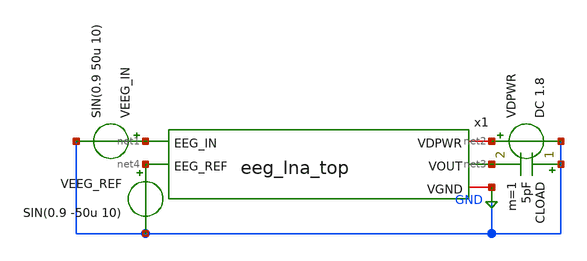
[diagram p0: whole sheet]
** sch_path: xschem/tb_eeg_lna_top.sch
**.subckt tb_eeg_lna_top
x1 net1 net2 net3 GND net4 eeg_lna_top
VDPWR net2 GND DC 1.8
VEEG_REF net4 GND SIN(0.9 -50u 10)
VEEG_IN net1 GND SIN(0.9 50u 10)
CLOAD GND net3 5pF m=1
**** begin user architecture code


.lib /foss/pdks/sky130A/libs.tech/ngspice/sky130.lib.spice tt

* =====================================================
* PARAMETERS
* =====================================================

.param VCM=0.9
.param VAMP=50u
.param FREQ=10

.option savecurrents

.control

* =====================================================
* DC OPERATING POINT
* =====================================================

op

print v(vcm)
print v(ota_inp)
print v(ota_inn)
print v(vout)

* =====================================================
* TRANSIENT ANALYSIS
* =====================================================

tran 100u 1

plot v(eeg_in) v(eeg_ref)
plot v(ota_inp) v(ota_inn)
plot v(vout)
plot v(vout)-0.9

* =====================================================
* AC ANALYSIS
* =====================================================

ac dec 100 0.01 1G

plot db(v(vout)/(v(eeg_in)-v(eeg_ref)))

.endc


**** end user architecture code
**.ends

* expanding   symbol:  eeg_lna_top.sym # of pins=5
** sym_path: xschem/eeg_lna_top.sym
** sch_path: xschem/eeg_lna_top.sch
.subckt eeg_lna_top EEG_IN VDPWR VOUT VGND EEG_REF
*.ipin EEG_IN
*.ipin EEG_REF
*.iopin VDPWR
*.iopin VGND
*.opin VOUT
XCIN_P EEG_IN OTA_INP sky130_fd_pr__cap_mim_m3_1 W=40 L=40 MF=1 m=1
XCIN_N EEG_REF OTA_INN sky130_fd_pr__cap_mim_m3_1 W=40 L=40 MF=1 m=1
x_ota net2 VDPWR OTA_INP OTA_INN VOUT VGND ota_5t
x_rpseudo_p net1 VCM OTA_INP pseudo_res_c
x_rpseudo_n net1 VCM OTA_INN pseudo_res_c
x_bias net2 VGND VDPWR bias_gen
x_vcm VDPWR VGND VCM vcm_gen
XCFB VOUT OTA_INN sky130_fd_pr__cap_mim_m3_1 W=20 L=20 MF=1 m=1
.ends


* expanding   symbol:  ota_5t.sym # of pins=6
** sym_path: xschem-new/ota_5t.sym
** sch_path: xschem-new/ota_5t.sch
.subckt ota_5t BIAS_P VDPWR VIN_P VIN_N VOUT VGND
*.ipin VIN_P
*.ipin VIN_N
*.ipin BIAS_P
*.iopin VDPWR
*.iopin VGND
*.opin VOUT
XMDIFF_P net1 VIN_P TAIL_P VDPWR sky130_fd_pr__pfet_01v8 L=4 W=48 nf=1 ad='int((1 + 1)/2) * 48 / 1 * 0.29'
+ as='int((1 + 2)/2) * 48 / 1 * 0.29' pd='2*int((1 + 1)/2) * (48 / 1 + 0.29)' ps='2*int((1 + 2)/2) * (48 / 1 + 0.29)'
+ nrd='0.29 / 48 ' nrs='0.29 / 48 ' sa=0 sb=0 sd=0 mult=1 m=1
XMDIFF_N VOUT VIN_N TAIL_P VDPWR sky130_fd_pr__pfet_01v8 L=4 W=48 nf=1 ad='int((1 + 1)/2) * 48 / 1 * 0.29'
+ as='int((1 + 2)/2) * 48 / 1 * 0.29' pd='2*int((1 + 1)/2) * (48 / 1 + 0.29)' ps='2*int((1 + 2)/2) * (48 / 1 + 0.29)'
+ nrd='0.29 / 48 ' nrs='0.29 / 48 ' sa=0 sb=0 sd=0 mult=1 m=1
XMTAIL TAIL_P BIAS_P VDPWR VDPWR sky130_fd_pr__pfet_01v8 L=8 W=0.5 nf=1 ad='int((1 + 1)/2) * 0.5 / 1 * 0.29'
+ as='int((1 + 2)/2) * 0.5 / 1 * 0.29' pd='2*int((1 + 1)/2) * (0.5 / 1 + 0.29)' ps='2*int((1 + 2)/2) * (0.5 / 1 + 0.29)'
+ nrd='0.29 / 0.5 ' nrs='0.29 / 0.5 ' sa=0 sb=0 sd=0 mult=1 m=1
XMLOAD_REF net1 net1 VGND VGND sky130_fd_pr__nfet_01v8 L=16 W=8 nf=1 ad='int((1 + 1)/2) * 8 / 1 * 0.29'
+ as='int((1 + 2)/2) * 8 / 1 * 0.29' pd='2*int((1 + 1)/2) * (8 / 1 + 0.29)' ps='2*int((1 + 2)/2) * (8 / 1 + 0.29)'
+ nrd='0.29 / 8 ' nrs='0.29 / 8 ' sa=0 sb=0 sd=0 mult=1 m=1
XMLOAD_OUT VOUT net1 VGND VGND sky130_fd_pr__nfet_01v8 L=16 W=8 nf=1 ad='int((1 + 1)/2) * 8 / 1 * 0.29'
+ as='int((1 + 2)/2) * 8 / 1 * 0.29' pd='2*int((1 + 1)/2) * (8 / 1 + 0.29)' ps='2*int((1 + 2)/2) * (8 / 1 + 0.29)'
+ nrd='0.29 / 8 ' nrs='0.29 / 8 ' sa=0 sb=0 sd=0 mult=1 m=1
.ends


* expanding   symbol:  pseudo_res_c.sym # of pins=3
** sym_path: xschem/pseudo_res_c.sym
** sch_path: xschem/pseudo_res_c.sch
.subckt pseudo_res_c VDPWR B A
*.iopin A
*.iopin B
*.iopin VDPWR
XP1 A net1 net1 VDPWR sky130_fd_pr__pfet_01v8 L=5 W=0.5 nf=1 ad='int((1 + 1)/2) * 0.5 / 1 * 0.29' as='int((1 + 2)/2) * 0.5 / 1 * 0.29'
+ pd='2*int((1 + 1)/2) * (0.5 / 1 + 0.29)' ps='2*int((1 + 2)/2) * (0.5 / 1 + 0.29)' nrd='0.29 / 0.5 ' nrs='0.29 / 0.5 '
+ sa=0 sb=0 sd=0 mult=10 m=10
XP2 net1 net1 B VDPWR sky130_fd_pr__pfet_01v8 L=5 W=0.5 nf=1 ad='int((1 + 1)/2) * 0.5 / 1 * 0.29' as='int((1 + 2)/2) * 0.5 / 1 * 0.29'
+ pd='2*int((1 + 1)/2) * (0.5 / 1 + 0.29)' ps='2*int((1 + 2)/2) * (0.5 / 1 + 0.29)' nrd='0.29 / 0.5 ' nrs='0.29 / 0.5 '
+ sa=0 sb=0 sd=0 mult=10 m=10
.ends


* expanding   symbol:  bias_gen.sym # of pins=3
** sym_path: xschem/bias_gen.sym
** sch_path: xschem/bias_gen.sch
.subckt bias_gen BIAS_P VGND VDPWR
*.iopin VDPWR
*.iopin VGND
*.opin BIAS_P
XM_BIAS_P BIAS_P BIAS_P VDPWR VDPWR sky130_fd_pr__pfet_01v8 L=2 W=1 nf=1 ad='int((1 + 1)/2) * 1 / 1 * 0.29'
+ as='int((1 + 2)/2) * 1 / 1 * 0.29' pd='2*int((1 + 1)/2) * (1 / 1 + 0.29)' ps='2*int((1 + 2)/2) * (1 / 1 + 0.29)'
+ nrd='0.29 / 1 ' nrs='0.29 / 1 ' sa=0 sb=0 sd=0 mult=1 m=1
XM_BIAS_N BIAS_P BIAS_P VGND VGND sky130_fd_pr__nfet_01v8 L=2 W=0.5 nf=1 ad='int((1 + 1)/2) * 0.5 / 1 * 0.29'
+ as='int((1 + 2)/2) * 0.5 / 1 * 0.29' pd='2*int((1 + 1)/2) * (0.5 / 1 + 0.29)' ps='2*int((1 + 2)/2) * (0.5 / 1 + 0.29)'
+ nrd='0.29 / 0.5 ' nrs='0.29 / 0.5 ' sa=0 sb=0 sd=0 mult=1 m=1
.ends


* expanding   symbol:  vcm_gen.sym # of pins=3
** sym_path: xschem/vcm_gen.sym
** sch_path: xschem/vcm_gen.sch
.subckt vcm_gen VDPWR VGND VCM
*.iopin VGND
*.iopin VDPWR
*.opin VCM
XC_VCM VGND VCM sky130_fd_pr__cap_mim_m3_1 W=25 L=25 MF=1 m=1
XR_VCM_TOP VCM VDPWR VGND sky130_fd_pr__res_xhigh_po_0p35 L=175 mult=1 m=1
XR_VCM_BOTTOM VGND VCM VGND sky130_fd_pr__res_xhigh_po_0p35 L=175 mult=1 m=1
.ends

.GLOBAL GND
.end
